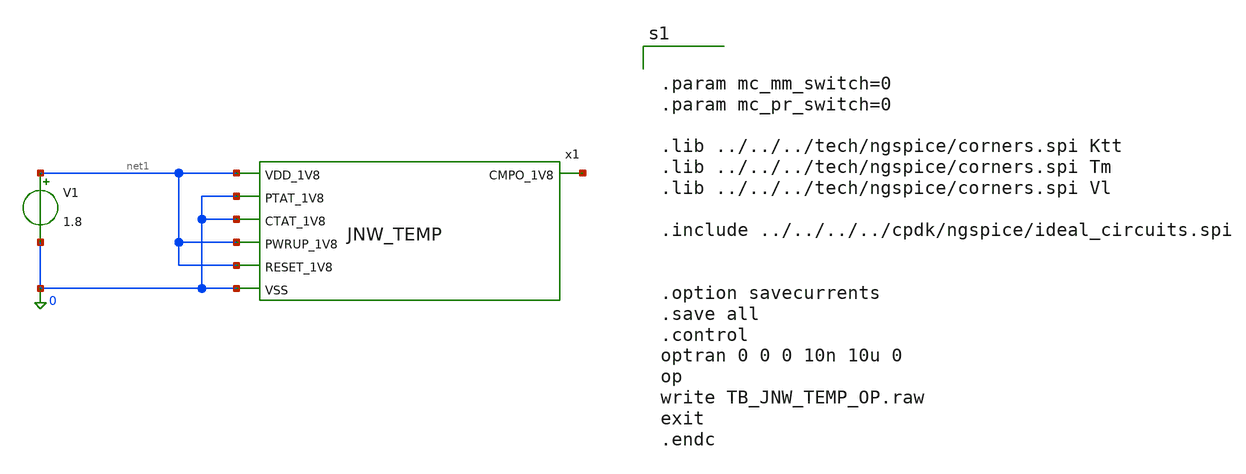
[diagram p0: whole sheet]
** sch_path: design/JNW_TEMP_SKY130A/TB_JNW_TEMP_OP.sch
**.subckt TB_JNW_TEMP_OP
x1 net1 0 0 net2 net1 net1 0 JNW_TEMP
V1 net1 0 1.8
**** begin user architecture code


.param mc_mm_switch=0
.param mc_pr_switch=0

.lib ../../../tech/ngspice/corners.spi Ktt
.lib ../../../tech/ngspice/corners.spi Tm
.lib ../../../tech/ngspice/corners.spi Vl

.include ../../../../cpdk/ngspice/ideal_circuits.spi


.option savecurrents
.save all
.control
optran 0 0 0 10n 10u 0
op
write TB_JNW_TEMP_OP.raw
exit
.endc



**** end user architecture code
**.ends
.end
